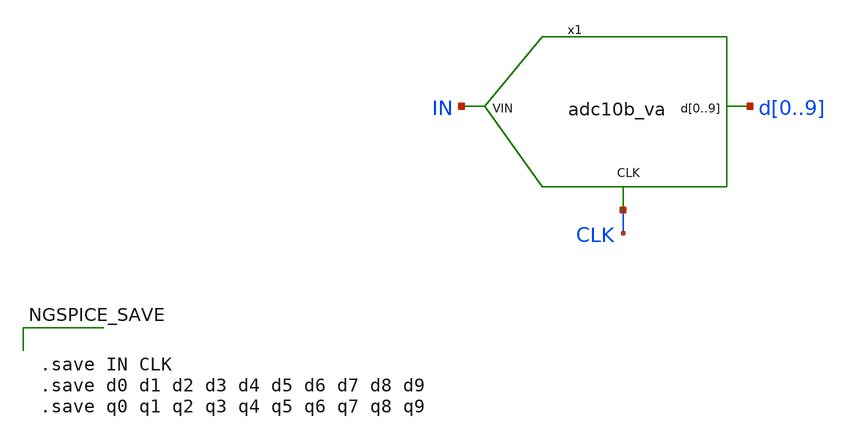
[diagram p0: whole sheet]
** sch_path: xschem/signal_test_2.sch
.lib $::SKYWATER_MODELS/sky130.lib.spice tt
.include $::SKYWATER_STDCELLS/sky130_fd_sc_hd.spice

**.subckt signal_test_2
x1 IN CLK d0 d1 d2 d3 d4 d5 d6 d7 d8 d9 adc10b_va
**** begin user architecture code



  *.options wnflag=0 bypass=1
  .option wnflag=1
  .option safecurrents
  *.option klu
  .options solver=klu nomod
  .options method=gear rawfile=binary
  .options reltol=1e-2

  .subckt adc10b_va in clk d0 d1 d2 d3 d4 d5 d6 d7 d8 d9
  N1 in clk d0 d1 d2 d3 d4 d5 d6 d7 d8 d9 adc_model
  .ends
  .model adc_model adc10bit
  ********************Static Voltage Sources***************************
  Vin in gnd SIN(0.9 0.9 9.95k)
  Vclk clk gnd pulse(1.8 0 10n 10n 0 5u 10u)

  VDD VDD gnd 1.8
  ********************Simulation Commands*****************************
  .control
     reset
     pre_osdi $THESIS_WS/verilogA/adc10bit.osdi
     set num_threads=8
     dc vin 0 1.8 0.0017578125
     *tran 10n 1m
     write signal_test_2-tb.raw
  .endc





.save IN CLK
.save d0 d1 d2 d3 d4 d5 d6 d7 d8 d9
.save q0 q1 q2 q3 q4 q5 q6 q7 q8 q9


**** end user architecture code
**.ends
.end
